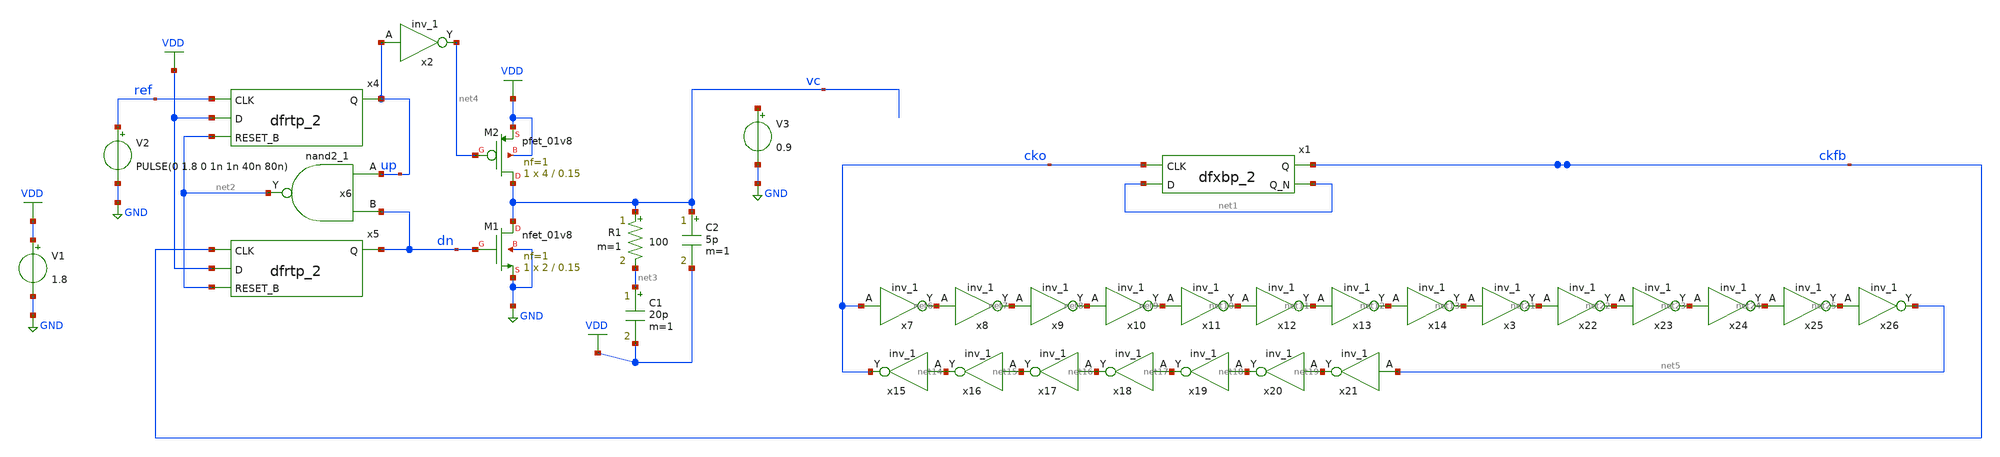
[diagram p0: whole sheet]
** sch_path: xschem/PLL_simple.sch
**.subckt PLL_simple
x1 cko net1 gnd gnd vdd vdd ckfb net1 sky130_fd_sc_hs__dfxbp_2
x4 ref VDD net2 gnd gnd vdd vdd up sky130_fd_sc_hs__dfrtp_2
x5 ckfb VDD net2 gnd gnd vdd vdd dn sky130_fd_sc_hs__dfrtp_2
x6 up dn gnd gnd vdd vdd net2 sky130_fd_sc_hs__nand2_1
V1 VDD GND 1.8
V2 ref GND PULSE(0 1.8 0 1n 1n 40n 80n)
XM1 vc dn GND GND sky130_fd_pr__nfet_01v8 L=0.15 W=2 nf=1 ad='int((nf+1)/2) * W/nf * 0.29' as='int((nf+2)/2) * W/nf * 0.29'
+ pd='2*int((nf+1)/2) * (W/nf + 0.29)' ps='2*int((nf+2)/2) * (W/nf + 0.29)' nrd='0.29 / W' nrs='0.29 / W'
+ sa=0 sb=0 sd=0 mult=1 m=1
XM2 vc net4 VDD VDD sky130_fd_pr__pfet_01v8 L=0.15 W=4 nf=1 ad='int((nf+1)/2) * W/nf * 0.29' as='int((nf+2)/2) * W/nf * 0.29'
+ pd='2*int((nf+1)/2) * (W/nf + 0.29)' ps='2*int((nf+2)/2) * (W/nf + 0.29)' nrd='0.29 / W' nrs='0.29 / W'
+ sa=0 sb=0 sd=0 mult=1 m=1
C1 net3 VDD 20p m=1
R1 vc net3 100 m=1
C2 vc VDD 5p m=1
x7 cko gnd gnd vc vc net6 sky130_fd_sc_hs__inv_1
x8 net6 gnd gnd vc vc net7 sky130_fd_sc_hs__inv_1
x9 net7 gnd gnd vc vc net8 sky130_fd_sc_hs__inv_1
x10 net8 gnd gnd vc vc net9 sky130_fd_sc_hs__inv_1
x11 net9 gnd gnd vc vc net10 sky130_fd_sc_hs__inv_1
x12 net10 gnd gnd vc vc net11 sky130_fd_sc_hs__inv_1
x13 net11 gnd gnd vc vc net12 sky130_fd_sc_hs__inv_1
x14 net12 gnd gnd vc vc net13 sky130_fd_sc_hs__inv_1
x15 net14 gnd gnd vc vc cko sky130_fd_sc_hs__inv_1
x16 net15 gnd gnd vc vc net14 sky130_fd_sc_hs__inv_1
x17 net16 gnd gnd vc vc net15 sky130_fd_sc_hs__inv_1
x18 net17 gnd gnd vc vc net16 sky130_fd_sc_hs__inv_1
x19 net18 gnd gnd vc vc net17 sky130_fd_sc_hs__inv_1
x20 net19 gnd gnd vc vc net18 sky130_fd_sc_hs__inv_1
x21 net5 gnd gnd vc vc net19 sky130_fd_sc_hs__inv_1
x2 up gnd gnd vdd vdd net4 sky130_fd_sc_hs__inv_1
V3 net20 GND 0.9
x3 net13 gnd gnd vc vc net21 sky130_fd_sc_hs__inv_1
x22 net21 gnd gnd vc vc net22 sky130_fd_sc_hs__inv_1
x23 net22 gnd gnd vc vc net23 sky130_fd_sc_hs__inv_1
x24 net23 gnd gnd vc vc net24 sky130_fd_sc_hs__inv_1
x25 net24 gnd gnd vc vc net25 sky130_fd_sc_hs__inv_1
x26 net25 gnd gnd vc vc net5 sky130_fd_sc_hs__inv_1
**** begin user architecture code
.lib $::SKYWATER_MODELS/sky130.lib.spice tt
.include $::PDKPATH/libs.ref/sky130_fd_sc_hs/spice/sky130_fd_sc_hs.spice


.tran 1n 1000n
.control
run
display
.endc


**** end user architecture code
**.ends
.GLOBAL VDD
.GLOBAL GND
.end
